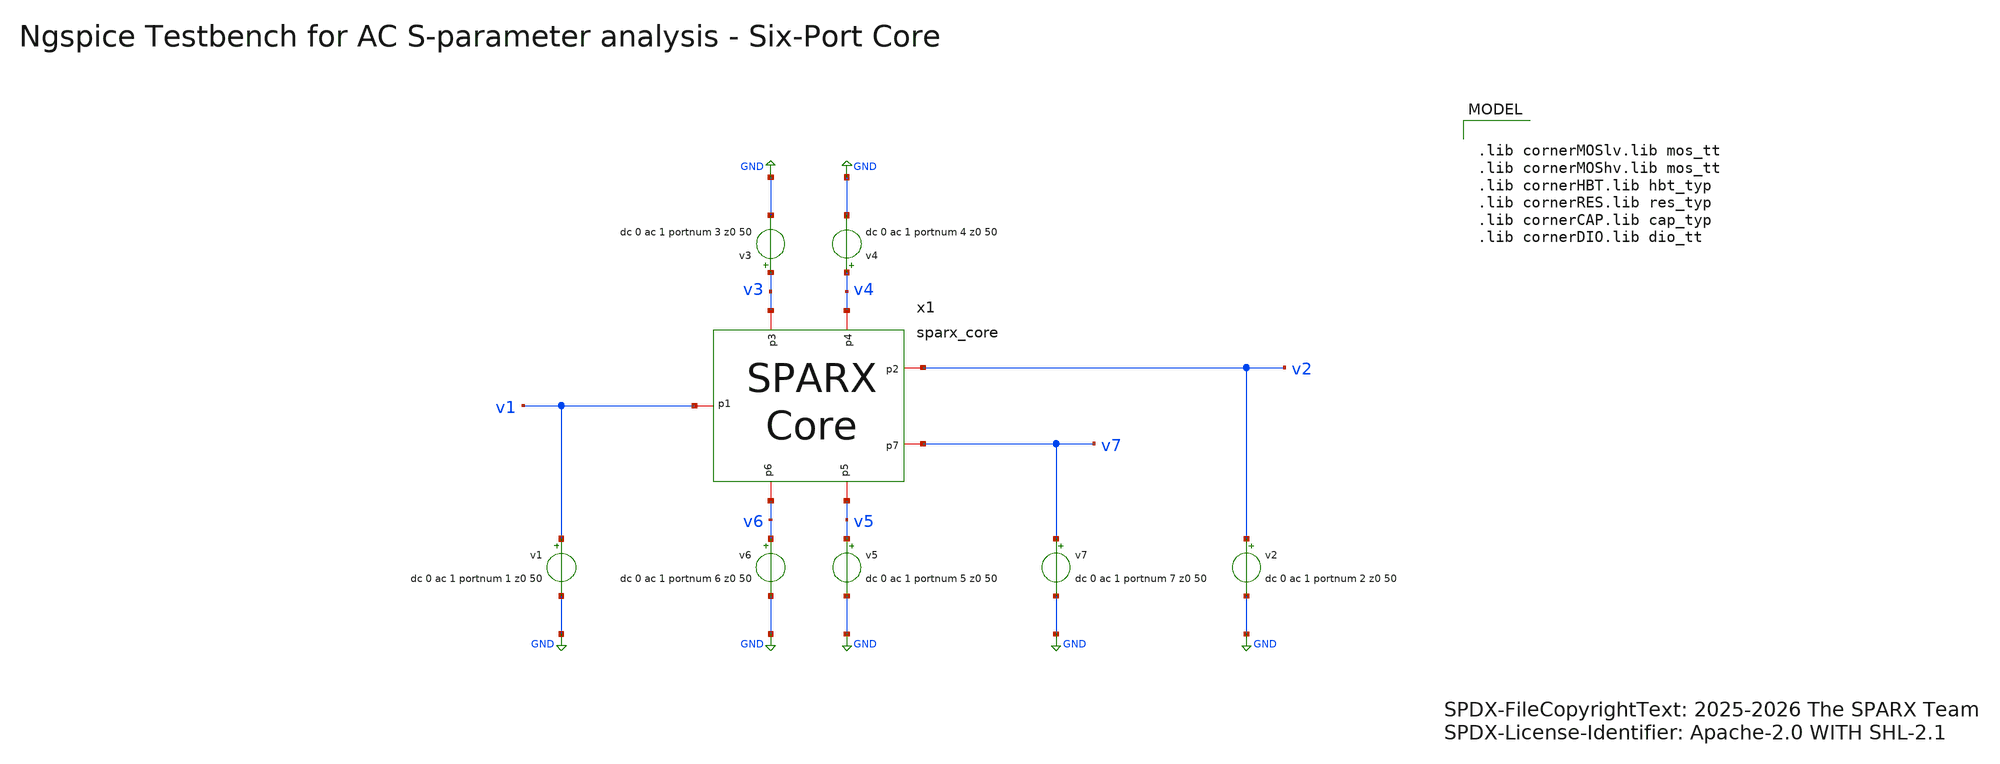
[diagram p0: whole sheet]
** sch_path: testbenches/xschem/sparx_core_tb_acsp_ngspice.sch
* SPDX-FileCopyrightText: 2025-2026 The SPARX Team
* SPDX-License-Identifier: Apache-2.0 WITH SHL-2.1
**.subckt sparx_core_tb_acsp_ngspice
v7 v7 GND dc 0 ac 1 portnum 7 z0 50
v2 v2 GND dc 0 ac 1 portnum 2 z0 50
x1 v3 v4 v2 v1 v7 v5 v6 sparx_core
v6 v6 GND dc 0 ac 1 portnum 6 z0 50
v5 v5 GND dc 0 ac 1 portnum 5 z0 50
v1 v1 GND dc 0 ac 1 portnum 1 z0 50
v4 v4 GND dc 0 ac 1 portnum 4 z0 50
v3 v3 GND dc 0 ac 1 portnum 3 z0 50
**** begin user architecture code


.include ../../../netlist/spice/sparx_bpf_le.spice
.include ../../../netlist/spice/sparx_wpd_le.spice
.include ../../../netlist/spice/sparx_blc_le.spice
.include ../sim_range.spice
.param temp=27
.options savecurrents klu method=gear reltol=1e-3 abstol=1e-15 gmin=1e-15
.control

save all

set wr_vecnames
set wr_singlescale

* User Constants
* f_min / f_max come from ../sim_range.spice (.csparam),
* auto-synced to the loaded Touchstone by snp2le.
* edit that file for a standalone run.

* Operating Point Analysis
op
remzerovec
write @schname\.raw
set appendwrite

* AC S-Parameter Analysis
sp lin 1001 $&const.f_min $&const.f_max
remzerovec

* Calculating S-Parameters
let s11_dB = db(S_1_1)
let s12_dB = db(S_1_2)
let s13_dB = db(S_1_3)
let s14_dB = db(S_1_4)
let s15_dB = db(S_1_5)
let s16_dB = db(S_1_6)
let s17_dB = db(S_1_7)
let s21_dB = db(S_2_1)
let s22_dB = db(S_2_2)
let s23_dB = db(S_2_3)
let s24_dB = db(S_2_4)
let s25_dB = db(S_2_5)
let s26_dB = db(S_2_6)
let s27_dB = db(S_2_7)
let s31_dB = db(S_3_1)
let s32_dB = db(S_3_2)
let s33_dB = db(S_3_3)
let s34_dB = db(S_3_4)
let s35_dB = db(S_3_5)
let s36_dB = db(S_3_6)
let s37_dB = db(S_3_7)
let s41_dB = db(S_4_1)
let s42_dB = db(S_4_2)
let s43_dB = db(S_4_3)
let s44_dB = db(S_4_4)
let s45_dB = db(S_4_5)
let s46_dB = db(S_4_6)
let s47_dB = db(S_4_7)
let s51_dB = db(S_5_1)
let s52_dB = db(S_5_2)
let s53_dB = db(S_5_3)
let s54_dB = db(S_5_4)
let s55_dB = db(S_5_5)
let s56_dB = db(S_5_6)
let s57_dB = db(S_5_7)
let s61_dB = db(S_6_1)
let s62_dB = db(S_6_2)
let s63_dB = db(S_6_3)
let s64_dB = db(S_6_4)
let s65_dB = db(S_6_5)
let s66_dB = db(S_6_6)
let s67_dB = db(S_6_7)
let s71_dB = db(S_7_1)
let s72_dB = db(S_7_2)
let s73_dB = db(S_7_3)
let s74_dB = db(S_7_4)
let s75_dB = db(S_7_5)
let s76_dB = db(S_7_6)
let s77_dB = db(S_7_7)
let s41_31_dB = s41_dB - s31_dB
let s51_61_dB = s51_dB - s61_dB
let s32_42_dB = s32_dB - s42_dB
let s62_52_dB = s62_dB - s52_dB

let s11_deg = cph(S_1_1) * 180/pi
let s12_deg = cph(S_1_2) * 180/pi
let s13_deg = cph(S_1_3) * 180/pi
let s14_deg = cph(S_1_4) * 180/pi
let s15_deg = cph(S_1_5) * 180/pi
let s16_deg = cph(S_1_6) * 180/pi
let s17_deg = cph(S_1_7) * 180/pi
let s21_deg = cph(S_2_1) * 180/pi
let s22_deg = cph(S_2_2) * 180/pi
let s23_deg = cph(S_2_3) * 180/pi
let s24_deg = cph(S_2_4) * 180/pi
let s25_deg = cph(S_2_5) * 180/pi
let s26_deg = cph(S_2_6) * 180/pi
let s27_deg = cph(S_2_7) * 180/pi
let s31_deg = cph(S_3_1) * 180/pi
let s32_deg = cph(S_3_2) * 180/pi
let s33_deg = cph(S_3_3) * 180/pi
let s34_deg = cph(S_3_4) * 180/pi
let s35_deg = cph(S_3_5) * 180/pi
let s36_deg = cph(S_3_6) * 180/pi
let s37_deg = cph(S_3_7) * 180/pi
let s41_deg = cph(S_4_1) * 180/pi
let s42_deg = cph(S_4_2) * 180/pi
let s43_deg = cph(S_4_3) * 180/pi
let s44_deg = cph(S_4_4) * 180/pi
let s45_deg = cph(S_4_5) * 180/pi
let s46_deg = cph(S_4_6) * 180/pi
let s47_deg = cph(S_4_7) * 180/pi
let s51_deg = cph(S_5_1) * 180/pi
let s52_deg = cph(S_5_2) * 180/pi
let s53_deg = cph(S_5_3) * 180/pi
let s54_deg = cph(S_5_4) * 180/pi
let s55_deg = cph(S_5_5) * 180/pi
let s56_deg = cph(S_5_6) * 180/pi
let s57_deg = cph(S_5_7) * 180/pi
let s61_deg = cph(S_6_1) * 180/pi
let s62_deg = cph(S_6_2) * 180/pi
let s63_deg = cph(S_6_3) * 180/pi
let s64_deg = cph(S_6_4) * 180/pi
let s65_deg = cph(S_6_5) * 180/pi
let s66_deg = cph(S_6_6) * 180/pi
let s67_deg = cph(S_6_7) * 180/pi
let s71_deg = cph(S_7_1) * 180/pi
let s72_deg = cph(S_7_2) * 180/pi
let s73_deg = cph(S_7_3) * 180/pi
let s74_deg = cph(S_7_4) * 180/pi
let s75_deg = cph(S_7_5) * 180/pi
let s76_deg = cph(S_7_6) * 180/pi
let s77_deg = cph(S_7_7) * 180/pi

let s41_31_deg = ph(S_4_1/S_3_1) * 180/pi
let s51_61_deg = ph(S_5_1/S_6_1) * 180/pi
let s32_42_deg = ph(S_3_2/S_4_2) * 180/pi
let s62_52_deg = ph(S_6_2/S_5_2) * 180/pi

* Write the raw AFTER the derived vectors so the interactive graphs can
* reference the imbalance vectors (s41_31_deg, ...) directly by name.
write @schname\.raw
set appendwrite

* Plotting
plot s11_dB s22_dB s33_dB s44_dB s55_dB s66_dB s77_dB
plot s41_31_dB s51_61_dB s32_42_dB s62_52_dB
plot s41_31_deg s51_61_deg s32_42_deg s62_52_deg

* Write Data
unset appendwrite
set wr_vecnames
set wr_singlescale
wrdata ../plot_simulations/data/@schname\.txt  s11_dB s12_dB s13_dB s14_dB s15_dB s16_dB s17_dB
+  s21_dB s22_dB s23_dB s24_dB s25_dB s26_dB s27_dB  s31_dB s32_dB s33_dB s34_dB s35_dB s36_dB s37_dB  s41_dB
+ s42_dB s43_dB s44_dB s45_dB s46_dB s47_dB  s51_dB s52_dB s53_dB s54_dB s55_dB s56_dB s57_dB  s61_dB s62_dB
+ s63_dB s64_dB s65_dB s66_dB s67_dB  s71_dB s72_dB s73_dB s74_dB s75_dB s76_dB s77_dB  s11_deg s12_deg
+ s13_deg s14_deg s15_deg s16_deg s17_deg  s21_deg s22_deg s23_deg s24_deg s25_deg s26_deg s27_deg  s31_deg
+ s32_deg s33_deg s34_deg s35_deg s36_deg s37_deg  s41_deg s42_deg s43_deg s44_deg s45_deg s46_deg s47_deg
+  s51_deg s52_deg s53_deg s54_deg s55_deg s56_deg s57_deg  s61_deg s62_deg s63_deg s64_deg s65_deg s66_deg
+ s67_deg  s71_deg s72_deg s73_deg s74_deg s75_deg s76_deg s77_deg  s41_31_dB s51_61_dB s32_42_dB s62_52_dB
+  s41_31_deg s51_61_deg s32_42_deg s62_52_deg

*quit
.endc



.lib cornerMOSlv.lib mos_tt
.lib cornerMOShv.lib mos_tt
.lib cornerHBT.lib hbt_typ
.lib cornerRES.lib res_typ
.lib cornerCAP.lib cap_typ
.lib cornerDIO.lib dio_tt

**** end user architecture code
**.ends

* expanding   symbol:  sparx_core.sym # of pins=7
** sym_path: schematic/sparx_core.sym
** sch_path: schematic/sparx_core.sch
.subckt sparx_core p3 p4 p2 p1 p7 p5 p6
*.iopin p1
*.iopin p3
*.iopin p4
*.iopin p2
*.iopin p7
*.iopin p6
*.iopin p5
x5 net3 net1 p4 p3 sparx_blc_le
x6 p2 p7 net2 net1 sparx_blc_le
x7 net5 net4 net3 sparx_wpd_le
x8 p1 net5 sparx_bpf_le
x4 net4 net2 p5 p6 sparx_blc_le
.ends

.GLOBAL GND
.end
